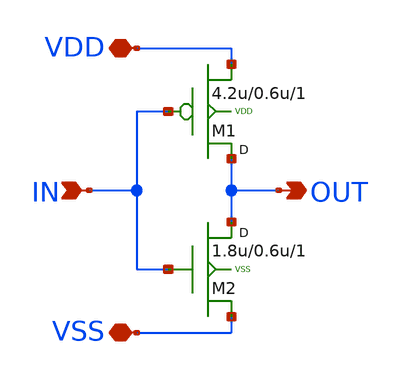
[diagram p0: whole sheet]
** sch_path: SRAM/inverter/schematic/inverter_schematic.sch
**.subckt inverter_schematic IN OUT VSS VDD
*.ipin IN
*.opin OUT
*.iopin VSS
*.iopin VDD
M2 OUT IN VSS VSS nfet w=1.8u l=0.6u m=1
M1 OUT IN VDD VDD pfet w=4.2u l=0.6u m=1
**.ends
.end
